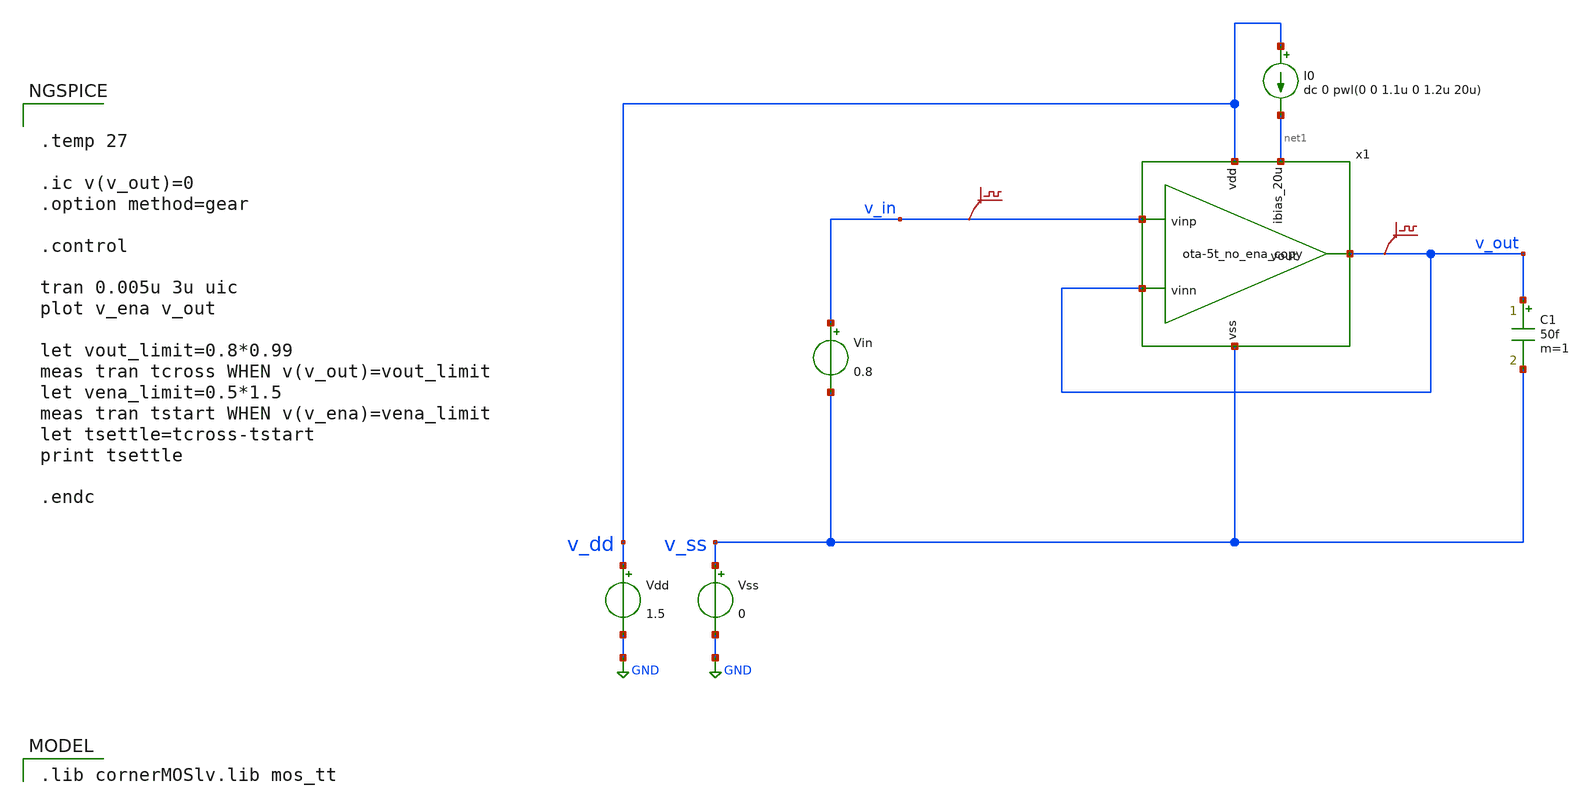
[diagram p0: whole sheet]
** sch_path: 004_Real_Circuits/002_version_no_enable/ota-5t_tb-tran_no_ena.sch
* (c) 2024-2025 Harald Pretl, Apache-2.0 license
**.subckt ota-5t_tb-tran_no_ena
Vdd v_dd GND 1.5
Vss v_ss GND 0
C1 v_out v_ss 50f m=1
Vin v_in v_ss 0.8
I0 v_dd net1 dc 0 pwl(0 0 1.1u 0 1.2u 20u)
.save v(v_in)
.save v(v_out)
x1 v_dd v_out v_in v_out net1 v_ss ota-5t_no_ena_copy
**** begin user architecture code
 .lib cornerMOSlv.lib mos_tt



.temp 27

.ic v(v_out)=0
.option method=gear

.control

tran 0.005u 3u uic
plot v_ena v_out

let vout_limit=0.8*0.99
meas tran tcross WHEN v(v_out)=vout_limit
let vena_limit=0.5*1.5
meas tran tstart WHEN v(v_ena)=vena_limit
let tsettle=tcross-tstart
print tsettle

.endc


**** end user architecture code
**.ends
.GLOBAL GND
.end
